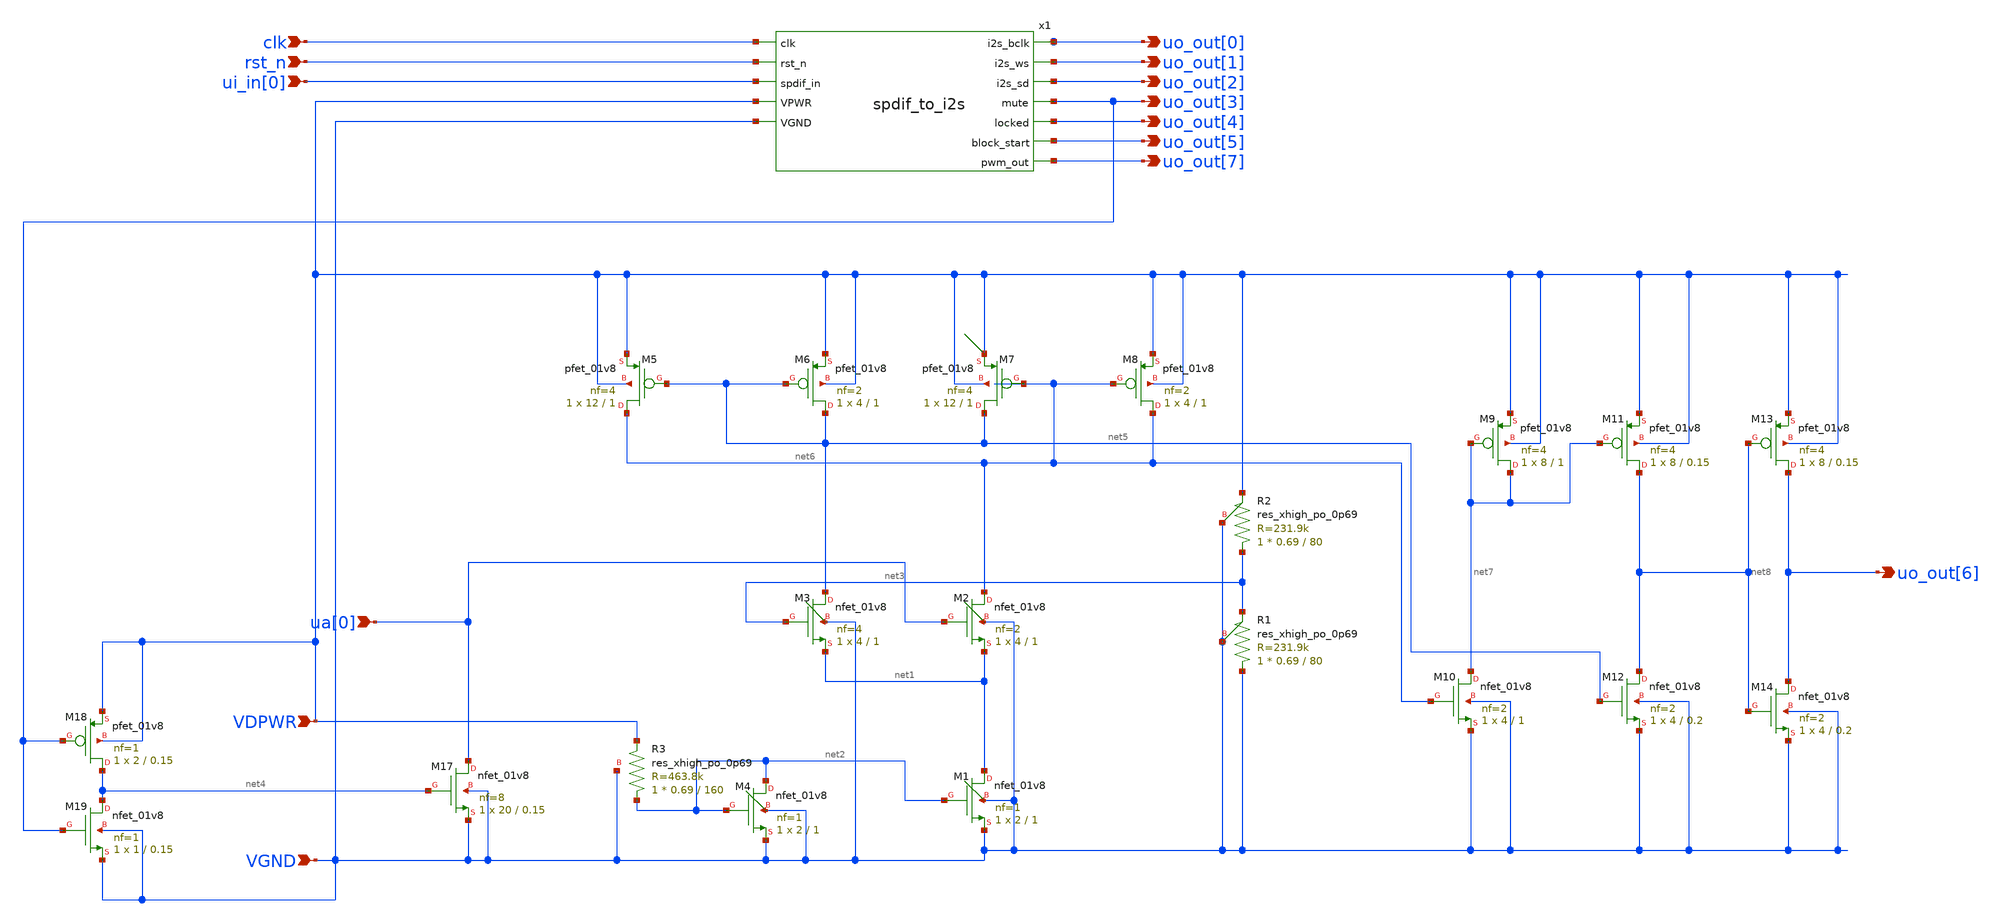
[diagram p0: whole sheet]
** sch_path: xschem/comp.sch
**.subckt comp ua[0] uo_out[6] VGND VDPWR ui_in[0] rst_n clk uo_out[0] uo_out[1] uo_out[2] uo_out[3]
*+ uo_out[4] uo_out[5] uo_out[7]
*.ipin ua[0]
*.opin uo_out[6]
*.ipin VGND
*.ipin VDPWR
*.ipin ui_in[0]
*.ipin rst_n
*.ipin clk
*.opin uo_out[0]
*.opin uo_out[1]
*.opin uo_out[2]
*.opin uo_out[3]
*.opin uo_out[4]
*.opin uo_out[5]
*.opin uo_out[7]
XM3 net5 net3 net1 VGND sky130_fd_pr__nfet_01v8 L=1 W=4 nf=4 ad='int((4 + 1)/2) * 4 / 4 * 0.29' as='int((4 + 2)/2) * 4 / 4 * 0.29'
+ pd='2*int((4 + 1)/2) * (4 / 4 + 0.29)' ps='2*int((4 + 2)/2) * (4 / 4 + 0.29)' nrd='0.29 / 4 ' nrs='0.29 / 4 '
+ sa=0 sb=0 sd=0 mult=1 m=1
XM2 net6 ua[0] net1 VGND sky130_fd_pr__nfet_01v8 L=1 W=4 nf=2 ad='int((2 + 1)/2) * 4 / 2 * 0.29' as='int((2 + 2)/2) * 4 / 2 * 0.29'
+ pd='2*int((2 + 1)/2) * (4 / 2 + 0.29)' ps='2*int((2 + 2)/2) * (4 / 2 + 0.29)' nrd='0.29 / 4 ' nrs='0.29 / 4 '
+ sa=0 sb=0 sd=0 mult=1 m=1
XM5 net6 net5 VDPWR VDPWR sky130_fd_pr__pfet_01v8 L=1 W=12 nf=4 ad='int((4 + 1)/2) * 12 / 4 * 0.29' as='int((4 + 2)/2) * 12 / 4 * 0.29'
+ pd='2*int((4 + 1)/2) * (12 / 4 + 0.29)' ps='2*int((4 + 2)/2) * (12 / 4 + 0.29)' nrd='0.29 / 12 ' nrs='0.29 / 12 '
+ sa=0 sb=0 sd=0 mult=1 m=1
XM4 net2 net2 VGND VGND sky130_fd_pr__nfet_01v8 L=1 W=2 nf=1 ad='int((1 + 1)/2) * 2 / 1 * 0.29' as='int((1 + 2)/2) * 2 / 1 * 0.29'
+ pd='2*int((1 + 1)/2) * (2 / 1 + 0.29)' ps='2*int((1 + 2)/2) * (2 / 1 + 0.29)' nrd='0.29 / 2 ' nrs='0.29 / 2 '
+ sa=0 sb=0 sd=0 mult=1 m=1
XM1 net1 net2 VGND VGND sky130_fd_pr__nfet_01v8 L=1 W=2 nf=1 ad='int((1 + 1)/2) * 2 / 1 * 0.29' as='int((1 + 2)/2) * 2 / 1 * 0.29'
+ pd='2*int((1 + 1)/2) * (2 / 1 + 0.29)' ps='2*int((1 + 2)/2) * (2 / 1 + 0.29)' nrd='0.29 / 2 ' nrs='0.29 / 2 '
+ sa=0 sb=0 sd=0 mult=1 m=1
XM17 ua[0] net4 VGND VGND sky130_fd_pr__nfet_01v8 L=0.15 W=20 nf=8 ad='int((8 + 1)/2) * 20 / 8 * 0.29'
+ as='int((8 + 2)/2) * 20 / 8 * 0.29' pd='2*int((8 + 1)/2) * (20 / 8 + 0.29)' ps='2*int((8 + 2)/2) * (20 / 8 + 0.29)'
+ nrd='0.29 / 20 ' nrs='0.29 / 20 ' sa=0 sb=0 sd=0 mult=1 m=1
XM18 net4 uo_out[3] VDPWR VDPWR sky130_fd_pr__pfet_01v8 L=0.15 W=2 nf=1 ad='int((1 + 1)/2) * 2 / 1 * 0.29'
+ as='int((1 + 2)/2) * 2 / 1 * 0.29' pd='2*int((1 + 1)/2) * (2 / 1 + 0.29)' ps='2*int((1 + 2)/2) * (2 / 1 + 0.29)'
+ nrd='0.29 / 2 ' nrs='0.29 / 2 ' sa=0 sb=0 sd=0 mult=1 m=1
XM19 net4 uo_out[3] VGND VGND sky130_fd_pr__nfet_01v8 L=0.15 W=1 nf=1 ad='int((1 + 1)/2) * 1 / 1 * 0.29'
+ as='int((1 + 2)/2) * 1 / 1 * 0.29' pd='2*int((1 + 1)/2) * (1 / 1 + 0.29)' ps='2*int((1 + 2)/2) * (1 / 1 + 0.29)'
+ nrd='0.29 / 1 ' nrs='0.29 / 1 ' sa=0 sb=0 sd=0 mult=1 m=1
XM6 net5 net5 VDPWR VDPWR sky130_fd_pr__pfet_01v8 L=1 W=4 nf=2 ad='int((2 + 1)/2) * 4 / 2 * 0.29' as='int((2 + 2)/2) * 4 / 2 * 0.29'
+ pd='2*int((2 + 1)/2) * (4 / 2 + 0.29)' ps='2*int((2 + 2)/2) * (4 / 2 + 0.29)' nrd='0.29 / 4 ' nrs='0.29 / 4 '
+ sa=0 sb=0 sd=0 mult=1 m=1
XM7 net5 net6 VDPWR VDPWR sky130_fd_pr__pfet_01v8 L=1 W=12 nf=4 ad='int((4 + 1)/2) * 12 / 4 * 0.29' as='int((4 + 2)/2) * 12 / 4 * 0.29'
+ pd='2*int((4 + 1)/2) * (12 / 4 + 0.29)' ps='2*int((4 + 2)/2) * (12 / 4 + 0.29)' nrd='0.29 / 12 ' nrs='0.29 / 12 '
+ sa=0 sb=0 sd=0 mult=1 m=1
XM8 net6 net6 VDPWR VDPWR sky130_fd_pr__pfet_01v8 L=1 W=4 nf=2 ad='int((2 + 1)/2) * 4 / 2 * 0.29' as='int((2 + 2)/2) * 4 / 2 * 0.29'
+ pd='2*int((2 + 1)/2) * (4 / 2 + 0.29)' ps='2*int((2 + 2)/2) * (4 / 2 + 0.29)' nrd='0.29 / 4 ' nrs='0.29 / 4 '
+ sa=0 sb=0 sd=0 mult=1 m=1
XM9 net7 net7 VDPWR VDPWR sky130_fd_pr__pfet_01v8 L=1 W=8 nf=4 ad='int((4 + 1)/2) * 8 / 4 * 0.29' as='int((4 + 2)/2) * 8 / 4 * 0.29'
+ pd='2*int((4 + 1)/2) * (8 / 4 + 0.29)' ps='2*int((4 + 2)/2) * (8 / 4 + 0.29)' nrd='0.29 / 8 ' nrs='0.29 / 8 '
+ sa=0 sb=0 sd=0 mult=1 m=1
XM10 net7 net6 VGND VGND sky130_fd_pr__nfet_01v8 L=1 W=4 nf=2 ad='int((2 + 1)/2) * 4 / 2 * 0.29' as='int((2 + 2)/2) * 4 / 2 * 0.29'
+ pd='2*int((2 + 1)/2) * (4 / 2 + 0.29)' ps='2*int((2 + 2)/2) * (4 / 2 + 0.29)' nrd='0.29 / 4 ' nrs='0.29 / 4 '
+ sa=0 sb=0 sd=0 mult=1 m=1
XM11 net8 net7 VDPWR VDPWR sky130_fd_pr__pfet_01v8 L=0.15 W=8 nf=4 ad='int((4 + 1)/2) * 8 / 4 * 0.29'
+ as='int((4 + 2)/2) * 8 / 4 * 0.29' pd='2*int((4 + 1)/2) * (8 / 4 + 0.29)' ps='2*int((4 + 2)/2) * (8 / 4 + 0.29)'
+ nrd='0.29 / 8 ' nrs='0.29 / 8 ' sa=0 sb=0 sd=0 mult=1 m=1
XM12 net8 net5 VGND VGND sky130_fd_pr__nfet_01v8 L=0.2 W=4 nf=2 ad='int((2 + 1)/2) * 4 / 2 * 0.29' as='int((2 + 2)/2) * 4 / 2 * 0.29'
+ pd='2*int((2 + 1)/2) * (4 / 2 + 0.29)' ps='2*int((2 + 2)/2) * (4 / 2 + 0.29)' nrd='0.29 / 4 ' nrs='0.29 / 4 '
+ sa=0 sb=0 sd=0 mult=1 m=1
XM13 uo_out[6] net8 VDPWR VDPWR sky130_fd_pr__pfet_01v8 L=0.15 W=8 nf=4 ad='int((4 + 1)/2) * 8 / 4 * 0.29'
+ as='int((4 + 2)/2) * 8 / 4 * 0.29' pd='2*int((4 + 1)/2) * (8 / 4 + 0.29)' ps='2*int((4 + 2)/2) * (8 / 4 + 0.29)'
+ nrd='0.29 / 8 ' nrs='0.29 / 8 ' sa=0 sb=0 sd=0 mult=1 m=1
XM14 uo_out[6] net8 VGND VGND sky130_fd_pr__nfet_01v8 L=0.2 W=4 nf=2 ad='int((2 + 1)/2) * 4 / 2 * 0.29'
+ as='int((2 + 2)/2) * 4 / 2 * 0.29' pd='2*int((2 + 1)/2) * (4 / 2 + 0.29)' ps='2*int((2 + 2)/2) * (4 / 2 + 0.29)'
+ nrd='0.29 / 4 ' nrs='0.29 / 4 ' sa=0 sb=0 sd=0 mult=1 m=1
x1 uo_out[5] clk uo_out[0] uo_out[2] uo_out[1] uo_out[4] uo_out[3] uo_out[7] rst_n ui_in[0] VGND
+ VDPWR spdif_to_i2s
XR1 VGND net3 VGND sky130_fd_pr__res_xhigh_po_0p69 L=80 mult=1 m=1
XR2 net3 VDPWR VGND sky130_fd_pr__res_xhigh_po_0p69 L=80 mult=1 m=1
XR3 net2 VDPWR VGND sky130_fd_pr__res_xhigh_po_0p69 L=160 mult=1 m=1
**.ends

* expanding   symbol:  spdif_to_i2s.sym # of pins=12
** sym_path: xschem/spdif_to_i2s.sym
.include ll/spdif_to_i2s.spice
.end
